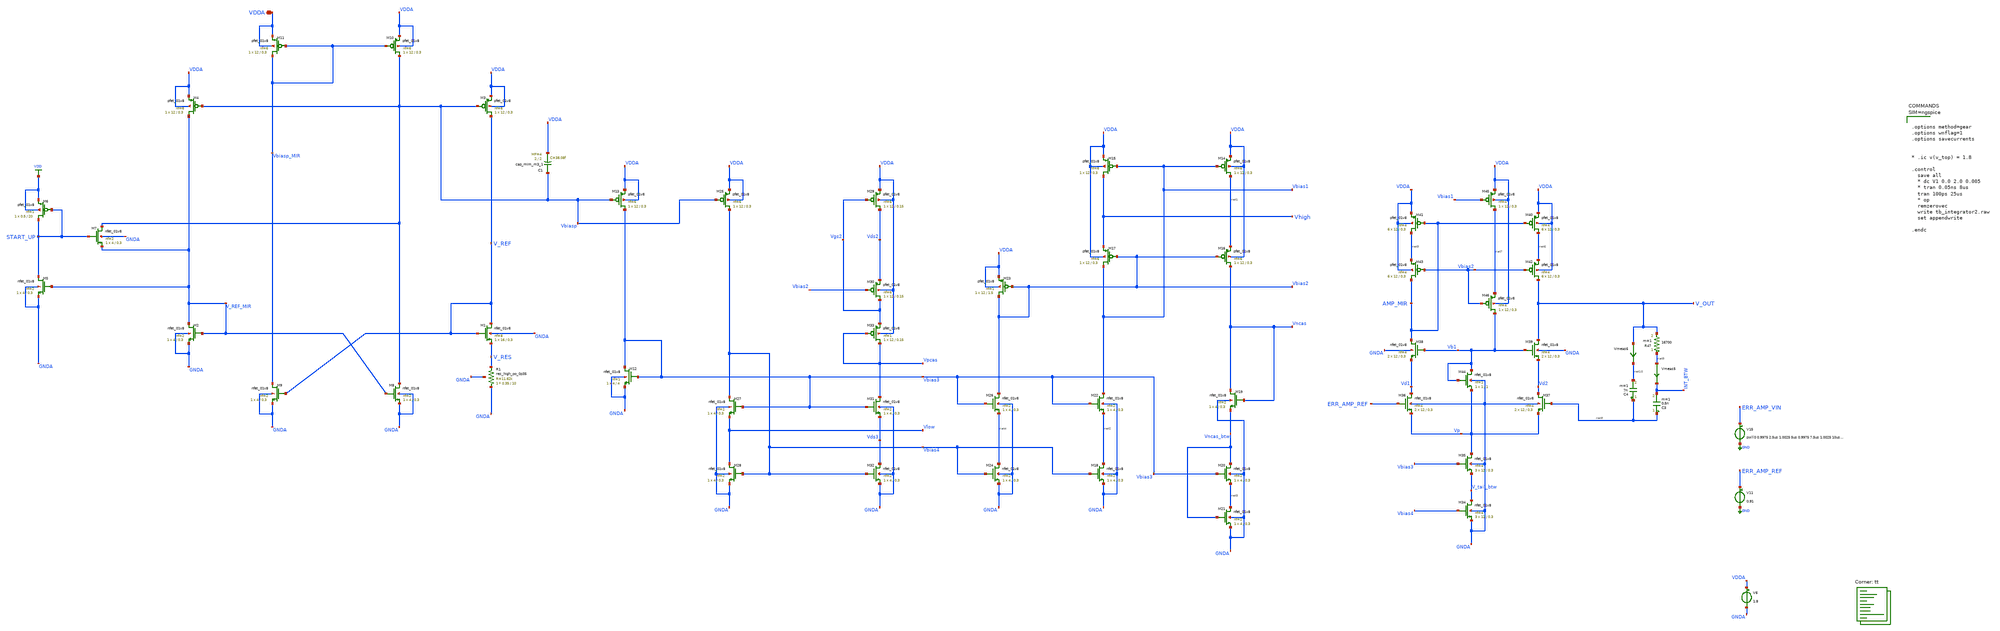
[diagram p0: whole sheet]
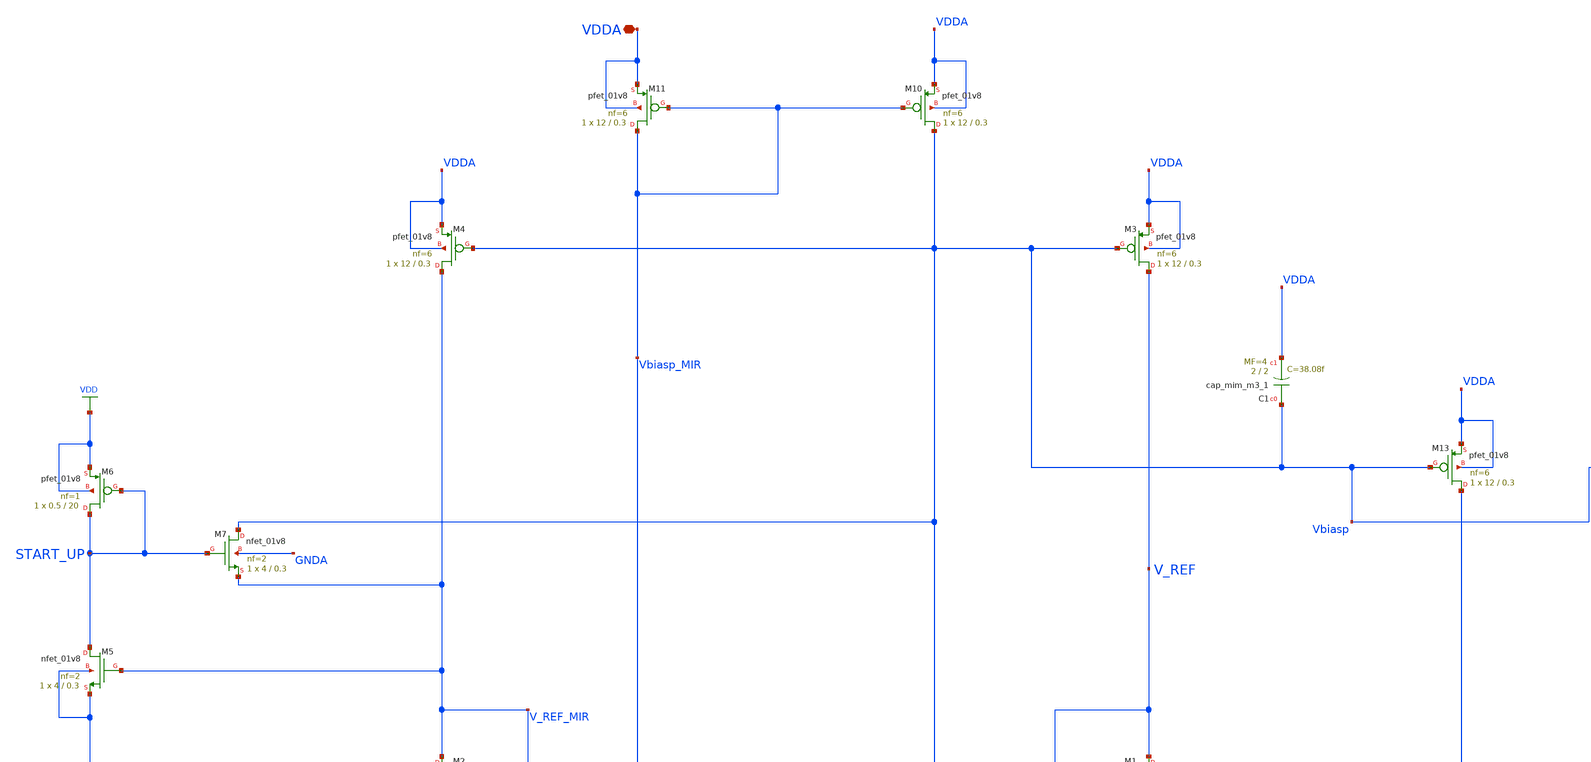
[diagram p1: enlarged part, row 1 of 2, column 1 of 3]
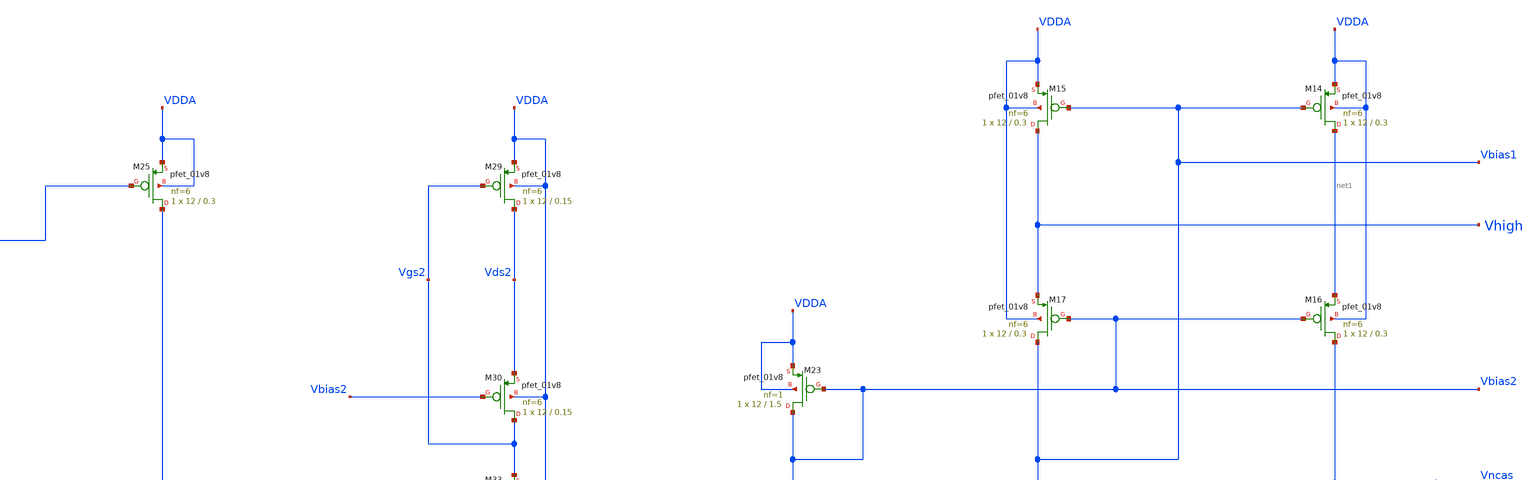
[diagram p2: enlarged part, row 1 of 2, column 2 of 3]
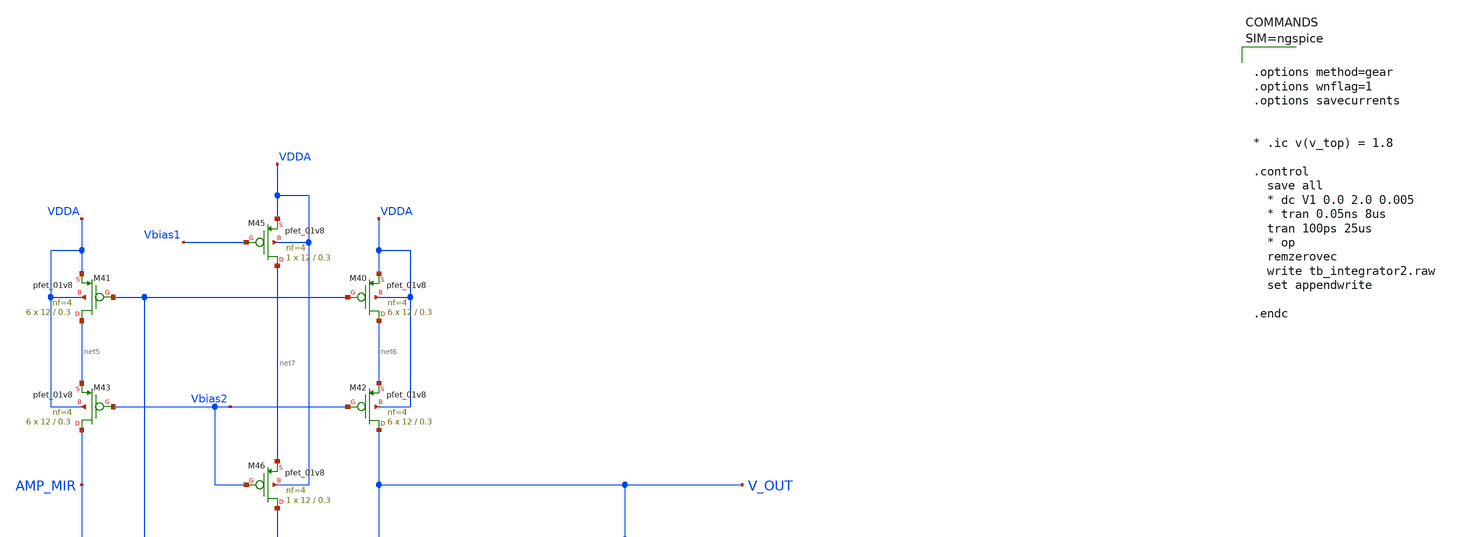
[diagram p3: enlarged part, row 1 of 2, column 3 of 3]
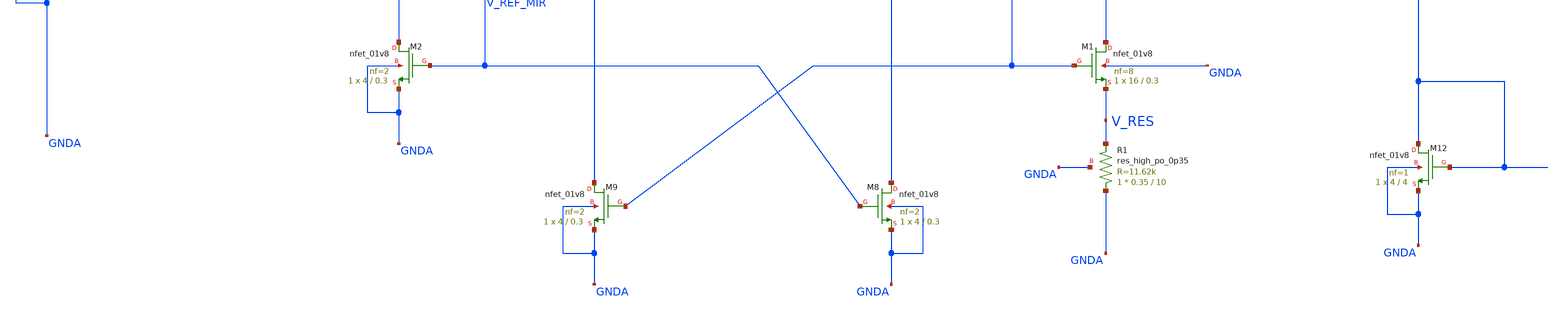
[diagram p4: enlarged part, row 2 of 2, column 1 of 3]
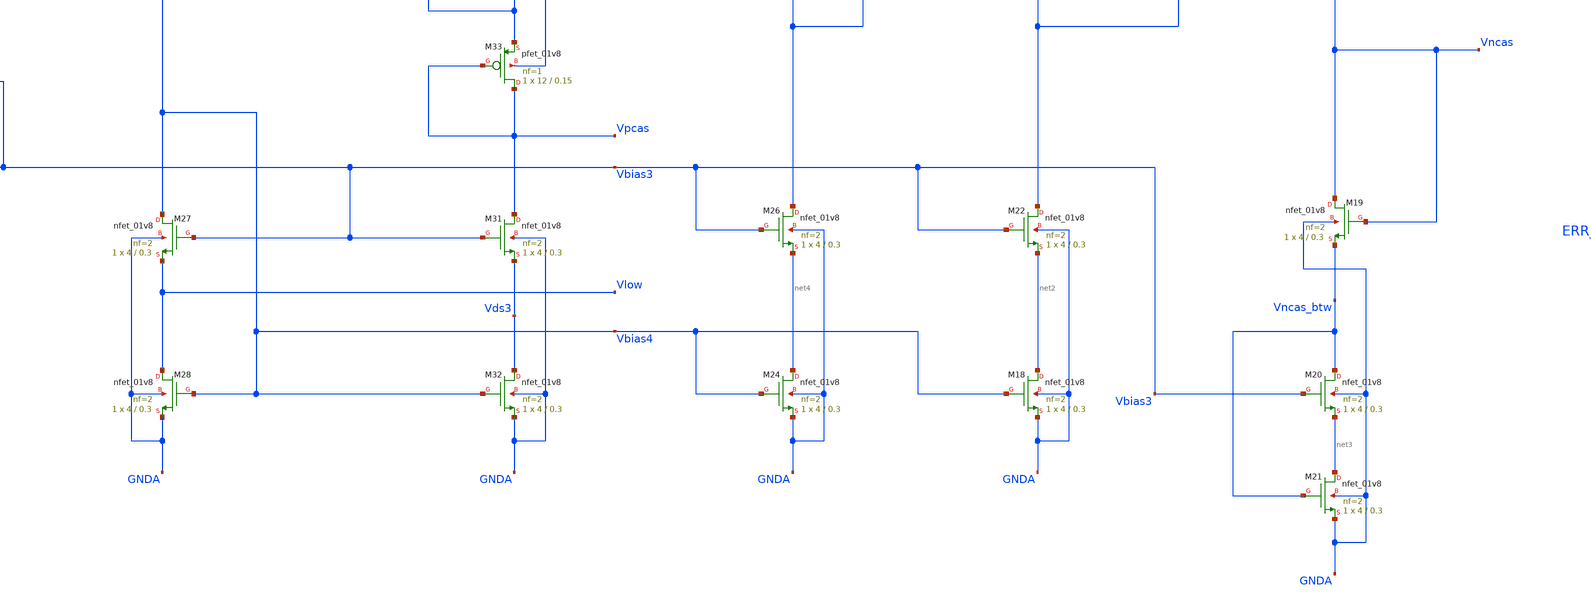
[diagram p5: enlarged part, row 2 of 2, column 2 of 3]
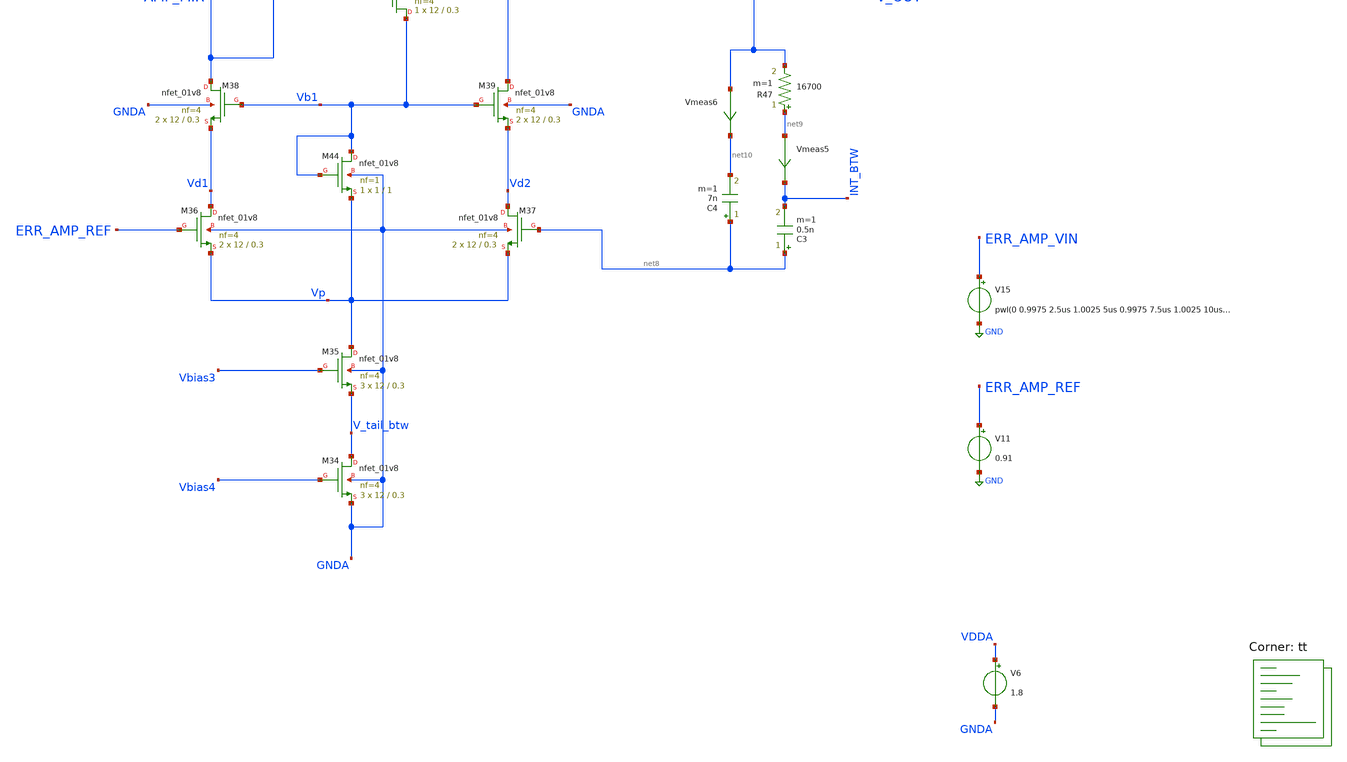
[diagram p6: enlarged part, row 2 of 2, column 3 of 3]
** sch_path: projects/ASU/EEE572/schematic/tb_integrator2.sch
**.subckt tb_integrator2 VDDA
*.iopin VDDA
V6 VDDA GNDA 1.8
V11 ERR_AMP_REF GND 0.91
V15 ERR_AMP_VIN GND pwl(0 0.9975 2.5us 1.0025 5us 0.9975 7.5us 1.0025 10us 0.9975 12.5us 1.0025 15us
+ 0.9975 17.5us 1.0025 20us 0.9975 22.5us 1.0025 25us 0.9975)
XM1 V_REF V_REF V_RES GNDA sky130_fd_pr__nfet_01v8 L=0.3 W=16 nf=8 ad='int((nf+1)/2) * W/nf * 0.29' as='int((nf+2)/2) * W/nf * 0.29'
+ pd='2*int((nf+1)/2) * (W/nf + 0.29)' ps='2*int((nf+2)/2) * (W/nf + 0.29)' nrd='0.29 / W' nrs='0.29 / W'
+ sa=0 sb=0 sd=0 mult=1 m=1
XM2 V_REF_MIR V_REF_MIR GNDA GNDA sky130_fd_pr__nfet_01v8 L=0.3 W=4 nf=2 ad='int((nf+1)/2) * W/nf * 0.29'
+ as='int((nf+2)/2) * W/nf * 0.29' pd='2*int((nf+1)/2) * (W/nf + 0.29)' ps='2*int((nf+2)/2) * (W/nf + 0.29)'
+ nrd='0.29 / W' nrs='0.29 / W' sa=0 sb=0 sd=0 mult=1 m=1
XM5 START_UP V_REF_MIR GNDA GNDA sky130_fd_pr__nfet_01v8 L=0.3 W=4 nf=2 ad='int((nf+1)/2) * W/nf * 0.29'
+ as='int((nf+2)/2) * W/nf * 0.29' pd='2*int((nf+1)/2) * (W/nf + 0.29)' ps='2*int((nf+2)/2) * (W/nf + 0.29)'
+ nrd='0.29 / W' nrs='0.29 / W' sa=0 sb=0 sd=0 mult=1 m=1
XM7 Vbiasp START_UP V_REF_MIR GNDA sky130_fd_pr__nfet_01v8 L=0.3 W=4 nf=2 ad='int((nf+1)/2) * W/nf * 0.29'
+ as='int((nf+2)/2) * W/nf * 0.29' pd='2*int((nf+1)/2) * (W/nf + 0.29)' ps='2*int((nf+2)/2) * (W/nf + 0.29)'
+ nrd='0.29 / W' nrs='0.29 / W' sa=0 sb=0 sd=0 mult=1 m=1
XM6 START_UP START_UP VDD VDD sky130_fd_pr__pfet_01v8 L=20 W=0.5 nf=1 ad='int((nf+1)/2) * W/nf * 0.29'
+ as='int((nf+2)/2) * W/nf * 0.29' pd='2*int((nf+1)/2) * (W/nf + 0.29)' ps='2*int((nf+2)/2) * (W/nf + 0.29)'
+ nrd='0.29 / W' nrs='0.29 / W' sa=0 sb=0 sd=0 mult=1 m=1
XM3 V_REF Vbiasp VDDA VDDA sky130_fd_pr__pfet_01v8 L=0.3 W=12 nf=6 ad='int((nf+1)/2) * W/nf * 0.29' as='int((nf+2)/2) * W/nf * 0.29'
+ pd='2*int((nf+1)/2) * (W/nf + 0.29)' ps='2*int((nf+2)/2) * (W/nf + 0.29)' nrd='0.29 / W' nrs='0.29 / W'
+ sa=0 sb=0 sd=0 mult=1 m=1
XM4 V_REF_MIR Vbiasp VDDA VDDA sky130_fd_pr__pfet_01v8 L=0.3 W=12 nf=6 ad='int((nf+1)/2) * W/nf * 0.29'
+ as='int((nf+2)/2) * W/nf * 0.29' pd='2*int((nf+1)/2) * (W/nf + 0.29)' ps='2*int((nf+2)/2) * (W/nf + 0.29)'
+ nrd='0.29 / W' nrs='0.29 / W' sa=0 sb=0 sd=0 mult=1 m=1
XM8 Vbiasp V_REF_MIR GNDA GNDA sky130_fd_pr__nfet_01v8 L=0.3 W=4 nf=2 ad='int((nf+1)/2) * W/nf * 0.29'
+ as='int((nf+2)/2) * W/nf * 0.29' pd='2*int((nf+1)/2) * (W/nf + 0.29)' ps='2*int((nf+2)/2) * (W/nf + 0.29)'
+ nrd='0.29 / W' nrs='0.29 / W' sa=0 sb=0 sd=0 mult=1 m=1
XM9 Vbiasp_MIR V_REF GNDA GNDA sky130_fd_pr__nfet_01v8 L=0.3 W=4 nf=2 ad='int((nf+1)/2) * W/nf * 0.29'
+ as='int((nf+2)/2) * W/nf * 0.29' pd='2*int((nf+1)/2) * (W/nf + 0.29)' ps='2*int((nf+2)/2) * (W/nf + 0.29)'
+ nrd='0.29 / W' nrs='0.29 / W' sa=0 sb=0 sd=0 mult=1 m=1
XM10 Vbiasp Vbiasp_MIR VDDA VDDA sky130_fd_pr__pfet_01v8 L=0.3 W=12 nf=6 ad='int((nf+1)/2) * W/nf * 0.29'
+ as='int((nf+2)/2) * W/nf * 0.29' pd='2*int((nf+1)/2) * (W/nf + 0.29)' ps='2*int((nf+2)/2) * (W/nf + 0.29)'
+ nrd='0.29 / W' nrs='0.29 / W' sa=0 sb=0 sd=0 mult=1 m=1
XM11 Vbiasp_MIR Vbiasp_MIR VDDA VDDA sky130_fd_pr__pfet_01v8 L=0.3 W=12 nf=6 ad='int((nf+1)/2) * W/nf * 0.29'
+ as='int((nf+2)/2) * W/nf * 0.29' pd='2*int((nf+1)/2) * (W/nf + 0.29)' ps='2*int((nf+2)/2) * (W/nf + 0.29)'
+ nrd='0.29 / W' nrs='0.29 / W' sa=0 sb=0 sd=0 mult=1 m=1
XM12 Vbias3 Vbias3 GNDA GNDA sky130_fd_pr__nfet_01v8 L=4 W=4 nf=1 ad='int((nf+1)/2) * W/nf * 0.29' as='int((nf+2)/2) * W/nf * 0.29'
+ pd='2*int((nf+1)/2) * (W/nf + 0.29)' ps='2*int((nf+2)/2) * (W/nf + 0.29)' nrd='0.29 / W' nrs='0.29 / W'
+ sa=0 sb=0 sd=0 mult=1 m=1
XM13 Vbias3 Vbiasp VDDA VDDA sky130_fd_pr__pfet_01v8 L=0.3 W=12 nf=6 ad='int((nf+1)/2) * W/nf * 0.29'
+ as='int((nf+2)/2) * W/nf * 0.29' pd='2*int((nf+1)/2) * (W/nf + 0.29)' ps='2*int((nf+2)/2) * (W/nf + 0.29)'
+ nrd='0.29 / W' nrs='0.29 / W' sa=0 sb=0 sd=0 mult=1 m=1
XM14 net1 Vbias1 VDDA VDDA sky130_fd_pr__pfet_01v8 L=0.3 W=12 nf=6 ad='int((nf+1)/2) * W/nf * 0.29' as='int((nf+2)/2) * W/nf * 0.29'
+ pd='2*int((nf+1)/2) * (W/nf + 0.29)' ps='2*int((nf+2)/2) * (W/nf + 0.29)' nrd='0.29 / W' nrs='0.29 / W'
+ sa=0 sb=0 sd=0 mult=1 m=1
XM15 Vhigh Vbias1 VDDA VDDA sky130_fd_pr__pfet_01v8 L=0.3 W=12 nf=6 ad='int((nf+1)/2) * W/nf * 0.29'
+ as='int((nf+2)/2) * W/nf * 0.29' pd='2*int((nf+1)/2) * (W/nf + 0.29)' ps='2*int((nf+2)/2) * (W/nf + 0.29)'
+ nrd='0.29 / W' nrs='0.29 / W' sa=0 sb=0 sd=0 mult=1 m=1
XM16 Vncas Vbias2 net1 VDDA sky130_fd_pr__pfet_01v8 L=0.3 W=12 nf=6 ad='int((nf+1)/2) * W/nf * 0.29'
+ as='int((nf+2)/2) * W/nf * 0.29' pd='2*int((nf+1)/2) * (W/nf + 0.29)' ps='2*int((nf+2)/2) * (W/nf + 0.29)'
+ nrd='0.29 / W' nrs='0.29 / W' sa=0 sb=0 sd=0 mult=1 m=1
XM17 Vbias1 Vbias2 Vhigh VDDA sky130_fd_pr__pfet_01v8 L=0.3 W=12 nf=6 ad='int((nf+1)/2) * W/nf * 0.29'
+ as='int((nf+2)/2) * W/nf * 0.29' pd='2*int((nf+1)/2) * (W/nf + 0.29)' ps='2*int((nf+2)/2) * (W/nf + 0.29)'
+ nrd='0.29 / W' nrs='0.29 / W' sa=0 sb=0 sd=0 mult=1 m=1
XM18 net2 Vbias4 GNDA GNDA sky130_fd_pr__nfet_01v8 L=0.3 W=4 nf=2 ad='int((nf+1)/2) * W/nf * 0.29' as='int((nf+2)/2) * W/nf * 0.29'
+ pd='2*int((nf+1)/2) * (W/nf + 0.29)' ps='2*int((nf+2)/2) * (W/nf + 0.29)' nrd='0.29 / W' nrs='0.29 / W'
+ sa=0 sb=0 sd=0 mult=1 m=1
XM19 Vncas Vncas Vncas_btw GNDA sky130_fd_pr__nfet_01v8 L=0.3 W=4 nf=2 ad='int((nf+1)/2) * W/nf * 0.29'
+ as='int((nf+2)/2) * W/nf * 0.29' pd='2*int((nf+1)/2) * (W/nf + 0.29)' ps='2*int((nf+2)/2) * (W/nf + 0.29)'
+ nrd='0.29 / W' nrs='0.29 / W' sa=0 sb=0 sd=0 mult=1 m=1
XM20 Vncas_btw Vbias3 net3 GNDA sky130_fd_pr__nfet_01v8 L=0.3 W=4 nf=2 ad='int((nf+1)/2) * W/nf * 0.29'
+ as='int((nf+2)/2) * W/nf * 0.29' pd='2*int((nf+1)/2) * (W/nf + 0.29)' ps='2*int((nf+2)/2) * (W/nf + 0.29)'
+ nrd='0.29 / W' nrs='0.29 / W' sa=0 sb=0 sd=0 mult=1 m=1
XM21 net3 Vncas_btw GNDA GNDA sky130_fd_pr__nfet_01v8 L=0.3 W=4 nf=2 ad='int((nf+1)/2) * W/nf * 0.29'
+ as='int((nf+2)/2) * W/nf * 0.29' pd='2*int((nf+1)/2) * (W/nf + 0.29)' ps='2*int((nf+2)/2) * (W/nf + 0.29)'
+ nrd='0.29 / W' nrs='0.29 / W' sa=0 sb=0 sd=0 mult=1 m=1
XM25 Vbias4 Vbiasp VDDA VDDA sky130_fd_pr__pfet_01v8 L=0.3 W=12 nf=6 ad='int((nf+1)/2) * W/nf * 0.29'
+ as='int((nf+2)/2) * W/nf * 0.29' pd='2*int((nf+1)/2) * (W/nf + 0.29)' ps='2*int((nf+2)/2) * (W/nf + 0.29)'
+ nrd='0.29 / W' nrs='0.29 / W' sa=0 sb=0 sd=0 mult=1 m=1
XM27 Vbias4 Vbias3 Vlow GNDA sky130_fd_pr__nfet_01v8 L=0.3 W=4 nf=2 ad='int((nf+1)/2) * W/nf * 0.29'
+ as='int((nf+2)/2) * W/nf * 0.29' pd='2*int((nf+1)/2) * (W/nf + 0.29)' ps='2*int((nf+2)/2) * (W/nf + 0.29)'
+ nrd='0.29 / W' nrs='0.29 / W' sa=0 sb=0 sd=0 mult=1 m=1
XM28 Vlow Vbias4 GNDA GNDA sky130_fd_pr__nfet_01v8 L=0.3 W=4 nf=2 ad='int((nf+1)/2) * W/nf * 0.29' as='int((nf+2)/2) * W/nf * 0.29'
+ pd='2*int((nf+1)/2) * (W/nf + 0.29)' ps='2*int((nf+2)/2) * (W/nf + 0.29)' nrd='0.29 / W' nrs='0.29 / W'
+ sa=0 sb=0 sd=0 mult=1 m=1
XM29 Vds2 Vgs2 VDDA VDDA sky130_fd_pr__pfet_01v8 L=0.15 W=12 nf=6 ad='int((nf+1)/2) * W/nf * 0.29' as='int((nf+2)/2) * W/nf * 0.29'
+ pd='2*int((nf+1)/2) * (W/nf + 0.29)' ps='2*int((nf+2)/2) * (W/nf + 0.29)' nrd='0.29 / W' nrs='0.29 / W'
+ sa=0 sb=0 sd=0 mult=1 m=1
XM30 Vgs2 Vbias2 Vds2 VDDA sky130_fd_pr__pfet_01v8 L=0.15 W=12 nf=6 ad='int((nf+1)/2) * W/nf * 0.29'
+ as='int((nf+2)/2) * W/nf * 0.29' pd='2*int((nf+1)/2) * (W/nf + 0.29)' ps='2*int((nf+2)/2) * (W/nf + 0.29)'
+ nrd='0.29 / W' nrs='0.29 / W' sa=0 sb=0 sd=0 mult=1 m=1
XM31 Vpcas Vbias3 Vds3 GNDA sky130_fd_pr__nfet_01v8 L=0.3 W=4 nf=2 ad='int((nf+1)/2) * W/nf * 0.29' as='int((nf+2)/2) * W/nf * 0.29'
+ pd='2*int((nf+1)/2) * (W/nf + 0.29)' ps='2*int((nf+2)/2) * (W/nf + 0.29)' nrd='0.29 / W' nrs='0.29 / W'
+ sa=0 sb=0 sd=0 mult=1 m=1
XM32 Vds3 Vbias4 GNDA GNDA sky130_fd_pr__nfet_01v8 L=0.3 W=4 nf=2 ad='int((nf+1)/2) * W/nf * 0.29' as='int((nf+2)/2) * W/nf * 0.29'
+ pd='2*int((nf+1)/2) * (W/nf + 0.29)' ps='2*int((nf+2)/2) * (W/nf + 0.29)' nrd='0.29 / W' nrs='0.29 / W'
+ sa=0 sb=0 sd=0 mult=1 m=1
XM33 Vpcas Vpcas Vgs2 VDDA sky130_fd_pr__pfet_01v8 L=0.15 W=12 nf=1 ad='int((nf+1)/2) * W/nf * 0.29'
+ as='int((nf+2)/2) * W/nf * 0.29' pd='2*int((nf+1)/2) * (W/nf + 0.29)' ps='2*int((nf+2)/2) * (W/nf + 0.29)'
+ nrd='0.29 / W' nrs='0.29 / W' sa=0 sb=0 sd=0 mult=1 m=1
XM22 Vbias1 Vbias3 net2 GNDA sky130_fd_pr__nfet_01v8 L=0.3 W=4 nf=2 ad='int((nf+1)/2) * W/nf * 0.29'
+ as='int((nf+2)/2) * W/nf * 0.29' pd='2*int((nf+1)/2) * (W/nf + 0.29)' ps='2*int((nf+2)/2) * (W/nf + 0.29)'
+ nrd='0.29 / W' nrs='0.29 / W' sa=0 sb=0 sd=0 mult=1 m=1
XM23 Vbias2 Vbias2 VDDA VDDA sky130_fd_pr__pfet_01v8 L=1.5 W=12 nf=1 ad='int((nf+1)/2) * W/nf * 0.29'
+ as='int((nf+2)/2) * W/nf * 0.29' pd='2*int((nf+1)/2) * (W/nf + 0.29)' ps='2*int((nf+2)/2) * (W/nf + 0.29)'
+ nrd='0.29 / W' nrs='0.29 / W' sa=0 sb=0 sd=0 mult=1 m=1
XM24 net4 Vbias4 GNDA GNDA sky130_fd_pr__nfet_01v8 L=0.3 W=4 nf=2 ad='int((nf+1)/2) * W/nf * 0.29' as='int((nf+2)/2) * W/nf * 0.29'
+ pd='2*int((nf+1)/2) * (W/nf + 0.29)' ps='2*int((nf+2)/2) * (W/nf + 0.29)' nrd='0.29 / W' nrs='0.29 / W'
+ sa=0 sb=0 sd=0 mult=1 m=1
XM26 Vbias2 Vbias3 net4 GNDA sky130_fd_pr__nfet_01v8 L=0.3 W=4 nf=2 ad='int((nf+1)/2) * W/nf * 0.29'
+ as='int((nf+2)/2) * W/nf * 0.29' pd='2*int((nf+1)/2) * (W/nf + 0.29)' ps='2*int((nf+2)/2) * (W/nf + 0.29)'
+ nrd='0.29 / W' nrs='0.29 / W' sa=0 sb=0 sd=0 mult=1 m=1
XC1 Vbiasp VDDA sky130_fd_pr__cap_mim_m3_1 W=2 L=2 MF=4 m=4
XR1 GNDA V_RES GNDA sky130_fd_pr__res_high_po_0p35 L=10 mult=1 m=1
XM34 V_tail_btw Vbias4 GNDA GNDA sky130_fd_pr__nfet_01v8 L=0.3 W=12 nf=4 ad='int((nf+1)/2) * W/nf * 0.29'
+ as='int((nf+2)/2) * W/nf * 0.29' pd='2*int((nf+1)/2) * (W/nf + 0.29)' ps='2*int((nf+2)/2) * (W/nf + 0.29)'
+ nrd='0.29 / W' nrs='0.29 / W' sa=0 sb=0 sd=0 mult=3 m=3
XM35 Vp Vbias3 V_tail_btw GNDA sky130_fd_pr__nfet_01v8 L=0.3 W=12 nf=4 ad='int((nf+1)/2) * W/nf * 0.29'
+ as='int((nf+2)/2) * W/nf * 0.29' pd='2*int((nf+1)/2) * (W/nf + 0.29)' ps='2*int((nf+2)/2) * (W/nf + 0.29)'
+ nrd='0.29 / W' nrs='0.29 / W' sa=0 sb=0 sd=0 mult=3 m=3
XM36 Vd1 ERR_AMP_REF Vp GNDA sky130_fd_pr__nfet_01v8 L=0.3 W=12 nf=4 ad='int((nf+1)/2) * W/nf * 0.29'
+ as='int((nf+2)/2) * W/nf * 0.29' pd='2*int((nf+1)/2) * (W/nf + 0.29)' ps='2*int((nf+2)/2) * (W/nf + 0.29)'
+ nrd='0.29 / W' nrs='0.29 / W' sa=0 sb=0 sd=0 mult=2 m=2
XM37 Vd2 net8 Vp GNDA sky130_fd_pr__nfet_01v8 L=0.3 W=12 nf=4 ad='int((nf+1)/2) * W/nf * 0.29' as='int((nf+2)/2) * W/nf * 0.29'
+ pd='2*int((nf+1)/2) * (W/nf + 0.29)' ps='2*int((nf+2)/2) * (W/nf + 0.29)' nrd='0.29 / W' nrs='0.29 / W'
+ sa=0 sb=0 sd=0 mult=2 m=2
XM38 AMP_MIR Vb1 Vd1 GNDA sky130_fd_pr__nfet_01v8 L=0.3 W=12 nf=4 ad='int((nf+1)/2) * W/nf * 0.29' as='int((nf+2)/2) * W/nf * 0.29'
+ pd='2*int((nf+1)/2) * (W/nf + 0.29)' ps='2*int((nf+2)/2) * (W/nf + 0.29)' nrd='0.29 / W' nrs='0.29 / W'
+ sa=0 sb=0 sd=0 mult=2 m=2
XM39 V_OUT Vb1 Vd2 GNDA sky130_fd_pr__nfet_01v8 L=0.3 W=12 nf=4 ad='int((nf+1)/2) * W/nf * 0.29' as='int((nf+2)/2) * W/nf * 0.29'
+ pd='2*int((nf+1)/2) * (W/nf + 0.29)' ps='2*int((nf+2)/2) * (W/nf + 0.29)' nrd='0.29 / W' nrs='0.29 / W'
+ sa=0 sb=0 sd=0 mult=2 m=2
XM40 net6 AMP_MIR VDDA VDDA sky130_fd_pr__pfet_01v8 L=0.3 W=12 nf=4 ad='int((nf+1)/2) * W/nf * 0.29'
+ as='int((nf+2)/2) * W/nf * 0.29' pd='2*int((nf+1)/2) * (W/nf + 0.29)' ps='2*int((nf+2)/2) * (W/nf + 0.29)'
+ nrd='0.29 / W' nrs='0.29 / W' sa=0 sb=0 sd=0 mult=6 m=6
XM41 net5 AMP_MIR VDDA VDDA sky130_fd_pr__pfet_01v8 L=0.3 W=12 nf=4 ad='int((nf+1)/2) * W/nf * 0.29'
+ as='int((nf+2)/2) * W/nf * 0.29' pd='2*int((nf+1)/2) * (W/nf + 0.29)' ps='2*int((nf+2)/2) * (W/nf + 0.29)'
+ nrd='0.29 / W' nrs='0.29 / W' sa=0 sb=0 sd=0 mult=6 m=6
XM42 V_OUT Vbias2 net6 VDDA sky130_fd_pr__pfet_01v8 L=0.3 W=12 nf=4 ad='int((nf+1)/2) * W/nf * 0.29'
+ as='int((nf+2)/2) * W/nf * 0.29' pd='2*int((nf+1)/2) * (W/nf + 0.29)' ps='2*int((nf+2)/2) * (W/nf + 0.29)'
+ nrd='0.29 / W' nrs='0.29 / W' sa=0 sb=0 sd=0 mult=6 m=6
XM43 AMP_MIR Vbias2 net5 VDDA sky130_fd_pr__pfet_01v8 L=0.3 W=12 nf=4 ad='int((nf+1)/2) * W/nf * 0.29'
+ as='int((nf+2)/2) * W/nf * 0.29' pd='2*int((nf+1)/2) * (W/nf + 0.29)' ps='2*int((nf+2)/2) * (W/nf + 0.29)'
+ nrd='0.29 / W' nrs='0.29 / W' sa=0 sb=0 sd=0 mult=6 m=6
XM44 Vb1 Vb1 Vp GNDA sky130_fd_pr__nfet_01v8 L=1 W=1 nf=1 ad='int((nf+1)/2) * W/nf * 0.29' as='int((nf+2)/2) * W/nf * 0.29'
+ pd='2*int((nf+1)/2) * (W/nf + 0.29)' ps='2*int((nf+2)/2) * (W/nf + 0.29)' nrd='0.29 / W' nrs='0.29 / W'
+ sa=0 sb=0 sd=0 mult=1 m=1
XM45 net7 Vbias1 VDDA VDDA sky130_fd_pr__pfet_01v8 L=0.3 W=12 nf=4 ad='int((nf+1)/2) * W/nf * 0.29' as='int((nf+2)/2) * W/nf * 0.29'
+ pd='2*int((nf+1)/2) * (W/nf + 0.29)' ps='2*int((nf+2)/2) * (W/nf + 0.29)' nrd='0.29 / W' nrs='0.29 / W'
+ sa=0 sb=0 sd=0 mult=1 m=1
XM46 Vb1 Vbias2 net7 VDDA sky130_fd_pr__pfet_01v8 L=0.3 W=12 nf=4 ad='int((nf+1)/2) * W/nf * 0.29' as='int((nf+2)/2) * W/nf * 0.29'
+ pd='2*int((nf+1)/2) * (W/nf + 0.29)' ps='2*int((nf+2)/2) * (W/nf + 0.29)' nrd='0.29 / W' nrs='0.29 / W'
+ sa=0 sb=0 sd=0 mult=1 m=1
C3 net8 INT_BTW 0.5n m=1
R47 net9 V_OUT 16700 m=1
C4 net8 net10 7n m=1
Vmeas5 net9 INT_BTW 0
.save i(vmeas5)
Vmeas6 V_OUT net10 0
.save i(vmeas6)
**** begin user architecture code
.lib $::SKYWATER_MODELS/sky130.lib.spice tt



.options method=gear
.options wnflag=1
.options savecurrents


* .ic v(v_top) = 1.8

.control
  save all
  * dc V1 0.0 2.0 0.005
  * tran 0.05ns 8us
  tran 100ps 25us
  * op
  remzerovec
  write tb_integrator2.raw
  set appendwrite

.endc





**** end user architecture code
**.ends
.GLOBAL GND
.GLOBAL VDD
.end
